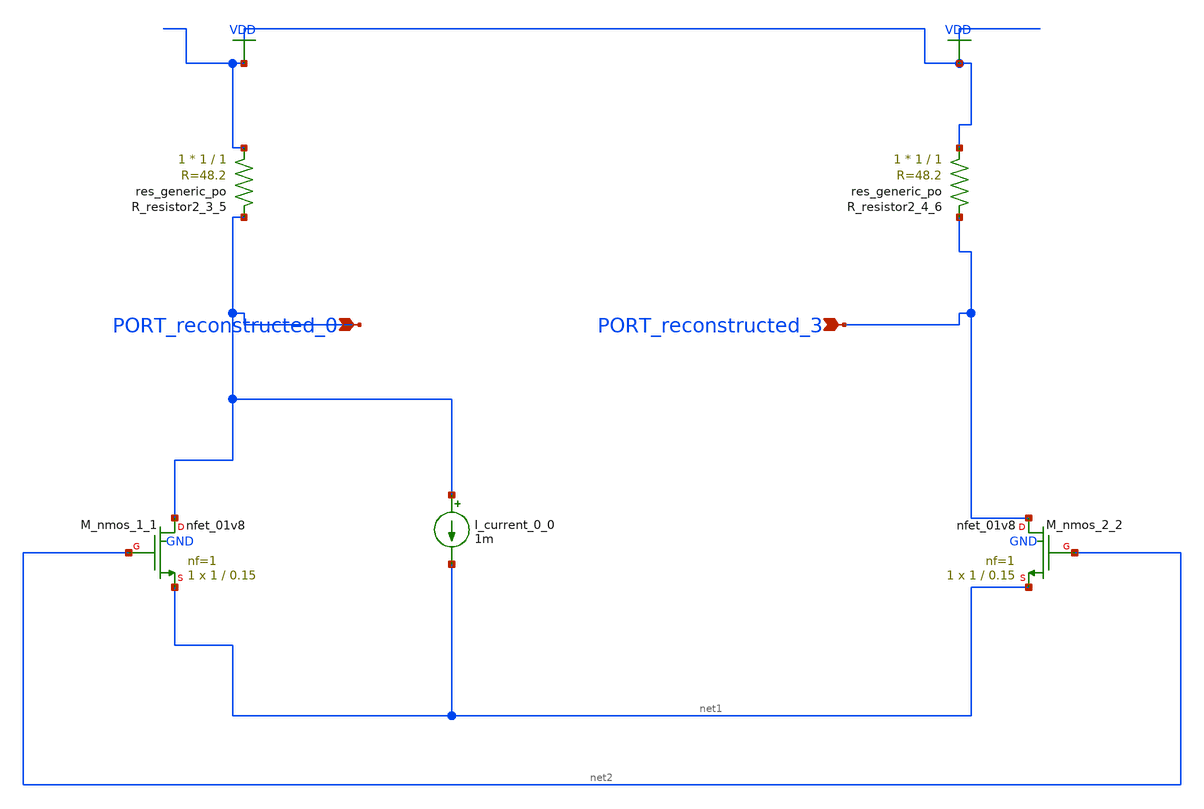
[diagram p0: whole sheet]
** sch_path: schematics/AMSNet/482.sch
**.subckt 482 PORT_reconstructed_0 PORT_reconstructed_3
*.ipin PORT_reconstructed_0
*.ipin PORT_reconstructed_3
I_current_0_0 PORT_reconstructed_0 net1 1m
XM_nmos_1_1 PORT_reconstructed_0 net2 net1 GND sky130_fd_pr__nfet_01v8 L=0.15 W=1 nf=1 ad='int((1 + 1)/2) * 1 / 1 * 0.29'
+ as='int((1 + 2)/2) * 1 / 1 * 0.29' pd='2*int((1 + 1)/2) * (1 / 1 + 0.29)' ps='2*int((1 + 2)/2) * (1 / 1 + 0.29)'
+ nrd='0.29 / 1 ' nrs='0.29 / 1 ' sa=0 sb=0 sd=0 mult=1 m=1
XM_nmos_2_2 PORT_reconstructed_3 net2 net1 GND sky130_fd_pr__nfet_01v8 L=0.15 W=1 nf=1 ad='int((1 + 1)/2) * 1 / 1 * 0.29'
+ as='int((1 + 2)/2) * 1 / 1 * 0.29' pd='2*int((1 + 1)/2) * (1 / 1 + 0.29)' ps='2*int((1 + 2)/2) * (1 / 1 + 0.29)'
+ nrd='0.29 / 1 ' nrs='0.29 / 1 ' sa=0 sb=0 sd=0 mult=1 m=1
XR_resistor2_3_5 VDD PORT_reconstructed_0 sky130_fd_pr__res_generic_po W=1 L=1 m=1
XR_resistor2_4_6 VDD PORT_reconstructed_3 sky130_fd_pr__res_generic_po W=1 L=1 m=1
**.ends
.GLOBAL VDD
.end
